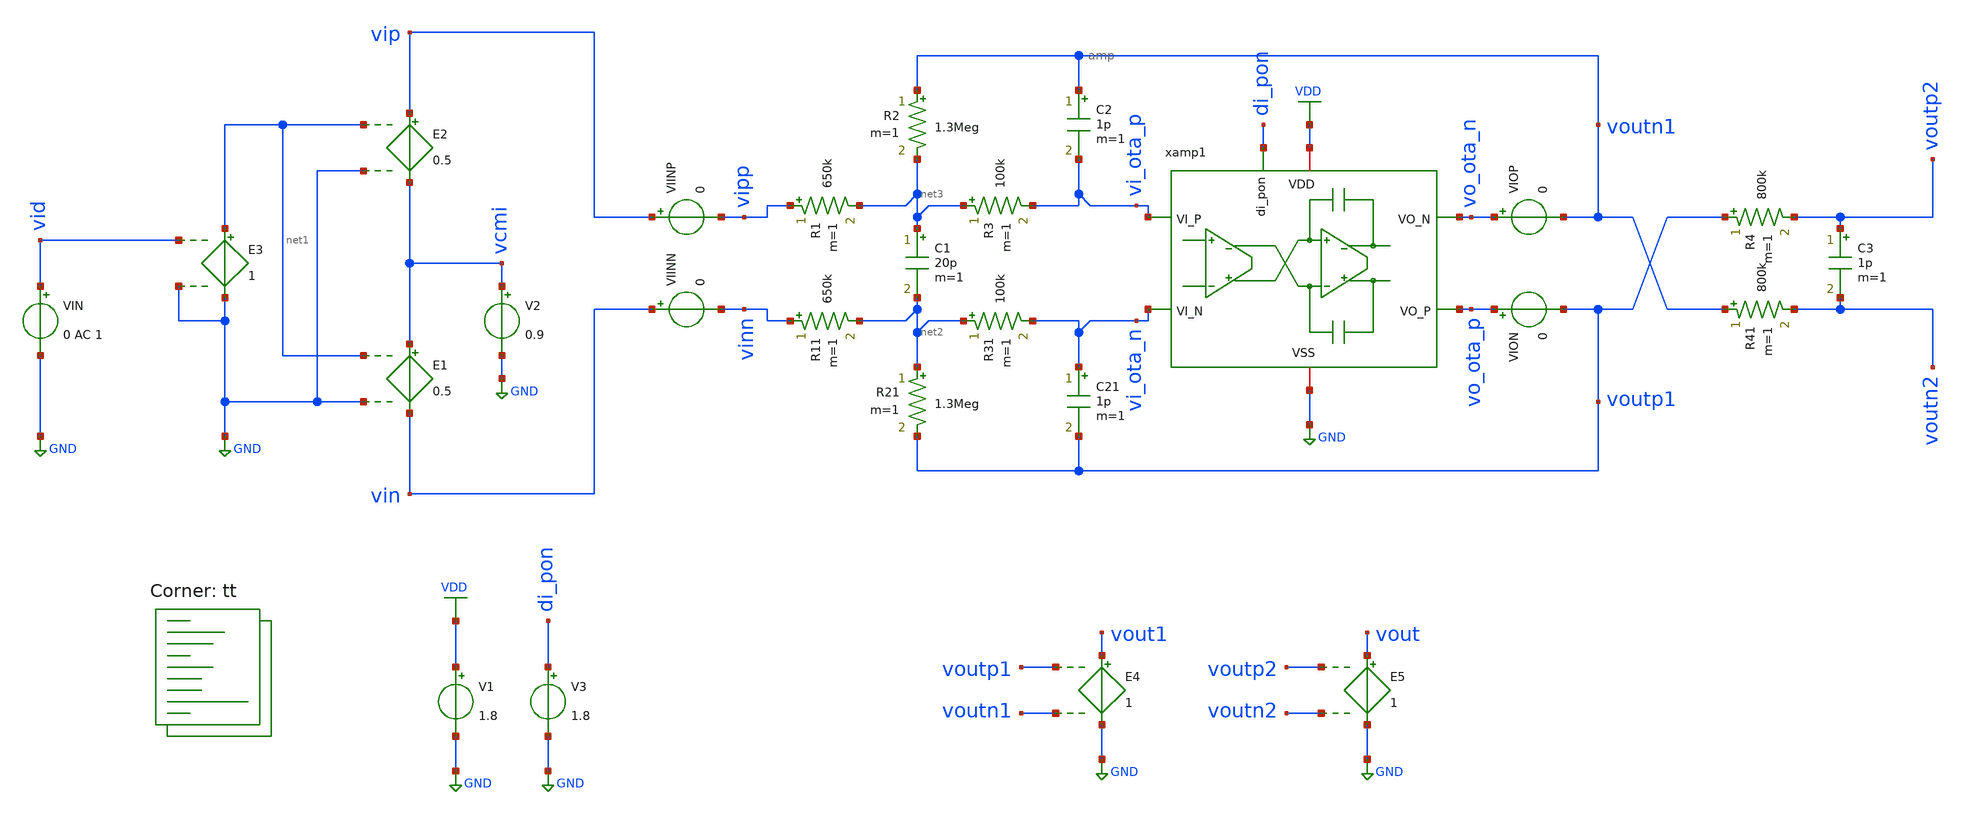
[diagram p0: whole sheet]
** sch_path: xschem/tb_filter_cl.sch
**.subckt tb_filter_cl
V2 vcmi GND 0.9
E1 vcmi vin net1 GND 0.5
E2 vip vcmi net1 GND 0.5
VIN vid GND 0 AC 1
E3 net1 GND vid GND 1
E4 vout1 GND voutp1 voutn1 1
VIINP vip vipp 0
VIINN vin vinn 0
R1 vipp net3 650k m=1
R2 voutn1 net3 1.3Meg m=1
R3 net3 vi_ota_p 100k m=1
C1 net3 net2 20p m=1
C3 voutp2 voutn2 1p m=1
R11 vinn net2 650k m=1
R21 net2 voutp1 1.3Meg m=1
R31 net2 vi_ota_n 100k m=1
C21 vi_ota_n voutp1 1p m=1
R4 voutp1 voutp2 800k m=1
R41 voutn1 voutn2 800k m=1
C2 voutn1 vi_ota_p 1p m=1
E5 vout GND voutp2 voutn2 1
VIOP vo_ota_n voutn1 0
VION vo_ota_p voutp1 0
xamp1 VDD vi_ota_n vi_ota_p vo_ota_p di_pon vo_ota_n GND amp
V1 VDD GND 1.8
V3 di_pon GND 1.8
**** begin user architecture code
.lib $::SKYWATER_MODELS/sky130.lib.spice tt


*.include /foss/designs/filter/amp_dev_save.spice
.options savecurrents
.options method=gear reltol=.005
.options sparse
.control
save all

let f_min = 10
let f_max = 100Meg
let f_stop = 500k

let Adc = 2
let err_gain_spec = 0.004
let v_step_o = 0.9
let v_step_i = v_step_o/Adc

let t_rf = 0.1u
let t_step = 50u
let t_delay = 0
let t_per = 2*t_step

let tstep = 0.1*t_rf
let tstop = 2*t_per
let tstart = t_delay

*alter @VIN[SIN] = [ 0 0.01 $&f_sig 0 0 0 ]
alter @VIN[DC] = 0.0


*set fndc = /foss/designs/frontend/frontend_dc.txt
*set fntran = /foss/designs/frontend/frontend_tran.txt
*set fnspec = /foss/designs/frontend/frontend_spec.txt
*set fnhd = /foss/designs/frontend/frontend_hd.txt
*set fnnoise = /foss/designs/frontend/frontend_noise.txt
set wr_singlescale
set wr_vecnames
option numdgt=3

set opSimOnly = 0


** Main Simulations
if $opSimOnly eq 0
	op
	ac dec 100 $&const.f_min $&const.f_max
	*set sqrnoise
	noise v(vout) VIN dec 100 $&const.f_min $&const.f_max 1
	noise v(vout) VIN dec 100 1 50Meg
	alter @VIN[PULSE] = [ 0 $&v_step_i $&t_delay $&t_rf $&t_rf $&t_step $&t_per 0 ]
	** Check power on by ramping Vdd, tie di_pon to VDD net!
	*alter @V1[PULSE] = [ 0 1.8 0 10u $&t_rf 0 0 0 ]
	tran $&tstep $&tstop $&tstart

	setplot ac1
	let A1 = v(vout1)/v(vid)
	let A2 = v(vout)/v(vid)

	let Amag_dB = vdb(A2)
	settype decibel Amag_dB
	let Aarg = 180/PI*cphase(A2)

	let fdc = const.f_min+1
	meas ac Adc_ol_dB find Amag_dB when frequency = fdc
	let Amag_fc = Adc_ol_dB-3
	meas ac fc find frequency when Amag_dB = Amag_fc
	meas ac Amin min_at Amag_dB from=const.f_min to=fc
	meas ac Amax max Amag_dB
	meas ac Astop find Amag_dB when frequency = const.f_stop

	meas ac fug find frequency when Amag_dB=0
	let err_gain_act = 1-10^(Adc_ol_dB/20)/Adc
	let Adc_ol_min = Adc*(1-err_gain_spec)/err_gain_spec
	let Adc_ol_min_dB = vdb(Adc_ol_min)
	print err_gain_act*100
	print Adc_ol_min_dB
	plot Amag_dB Aarg ylabel 'Magnitude, Phase'

	setplot noise1
	let acgain = onoise_spectrum/inoise_spectrum
	let r1 = sqrt(2)*onoise_r1
	let r2 = sqrt(2)*onoise_r2
	let r3 = sqrt(2)*onoise_r3
	let r4 = sqrt(2)*onoise_r4
	*plot inoise_spectrum ylog xlog
	plot onoise_spectrum r1 r2 r3 r4 ylog xlog ylabel 'Output Noise'

	setplot noise4
	let p_noise_q = (1e-3)^2
	let p_noise_o = onoise_total^2
	let p_sig_o = (v_step_o/(2*sqrt(2)))^2
	let snr = p_sig_o/(p_noise_o+p_noise_q)
	let snr_dB = 10*log10(snr)
	print snr_dB

	setplot tran4
	let vid = v(vid)
	let iop = viop#branch
	let ion = vion#branch
	let vcmo = (voutp1+voutn1)/2

	*plot iop ion

	plot vid vout1 vout vcmo
	plot v(vip) v(vin) v(voutp1) v(voutn1) vcmo
end

alter @VIN[DC] = 0
op

remzerovec
write tb_filter_cl.raw
.endc

**** end user architecture code
**.ends

* expanding   symbol:  /foss/designs/xschem/amp.sym # of pins=7
** sym_path: xschem/amp.sym
** sch_path: xschem/amp.sch
.subckt amp VDD VI_N VI_P VO_P di_pon VO_N VSS
*.iopin VSS
*.iopin VDD
*.ipin VI_P
*.ipin di_pon
*.ipin VI_N
*.opin VO_P
*.opin VO_N
XMP1 vbp vbp VDD VDD sky130_fd_pr__pfet_01v8 L=0.25 W='5 * 2 ' nf=2 ad='int((nf+1)/2) * W / nf * 0.29'
+ as='int((nf+2)/2) * W / nf * 0.29' pd='2*int((nf+1)/2) * (W / nf + 0.29)' ps='2*int((nf+2)/2) * (W / nf + 0.29)'
+ nrd='0.29 / W ' nrs='0.29 / W ' sa=0 sb=0 sd=0 mult=1 m=1
XMPSW3 vbp pon VDD VDD sky130_fd_pr__pfet_01v8 L=0.15 W='5 * 5 ' nf=5 ad='int((nf+1)/2) * W / nf * 0.29'
+ as='int((nf+2)/2) * W / nf * 0.29' pd='2*int((nf+1)/2) * (W / nf + 0.29)' ps='2*int((nf+2)/2) * (W / nf + 0.29)'
+ nrd='0.29 / W ' nrs='0.29 / W ' sa=0 sb=0 sd=0 mult=1 m=1
XMNSW1 pon_b di_pon VSS VSS sky130_fd_pr__nfet_01v8 L=0.15 W='3 * 1 ' nf=1 ad='int((nf+1)/2) * W / nf * 0.29'
+ as='int((nf+2)/2) * W / nf * 0.29' pd='2*int((nf+1)/2) * (W / nf + 0.29)' ps='2*int((nf+2)/2) * (W / nf + 0.29)'
+ nrd='0.29 / W ' nrs='0.29 / W ' sa=0 sb=0 sd=0 mult=1 m=1
XMPSW1 pon_b di_pon VDD VDD sky130_fd_pr__pfet_01v8 L=0.15 W='5 * 1 ' nf=1 ad='int((nf+1)/2) * W / nf * 0.29'
+ as='int((nf+2)/2) * W / nf * 0.29' pd='2*int((nf+1)/2) * (W / nf + 0.29)' ps='2*int((nf+2)/2) * (W / nf + 0.29)'
+ nrd='0.29 / W ' nrs='0.29 / W ' sa=0 sb=0 sd=0 mult=1 m=1
XMNSW2 pon pon_b VSS VSS sky130_fd_pr__nfet_01v8 L=0.15 W='3 * 3 ' nf=3 ad='int((nf+1)/2) * W / nf * 0.29'
+ as='int((nf+2)/2) * W / nf * 0.29' pd='2*int((nf+1)/2) * (W / nf + 0.29)' ps='2*int((nf+2)/2) * (W / nf + 0.29)'
+ nrd='0.29 / W ' nrs='0.29 / W ' sa=0 sb=0 sd=0 mult=1 m=1
XMPSW2 pon pon_b VDD VDD sky130_fd_pr__pfet_01v8 L=0.15 W='5 * 3 ' nf=3 ad='int((nf+1)/2) * W / nf * 0.29'
+ as='int((nf+2)/2) * W / nf * 0.29' pd='2*int((nf+1)/2) * (W / nf + 0.29)' ps='2*int((nf+2)/2) * (W / nf + 0.29)'
+ nrd='0.29 / W ' nrs='0.29 / W ' sa=0 sb=0 sd=0 mult=1 m=1
XMP2 viref1 vbp VDD VDD sky130_fd_pr__pfet_01v8 L=0.25 W='5 * 20 ' nf=20 ad='int((nf+1)/2) * W / nf * 0.29'
+ as='int((nf+2)/2) * W / nf * 0.29' pd='2*int((nf+1)/2) * (W / nf + 0.29)' ps='2*int((nf+2)/2) * (W / nf + 0.29)'
+ nrd='0.29 / W ' nrs='0.29 / W ' sa=0 sb=0 sd=0 mult=1 m=1
XC5 VDD vbp sky130_fd_pr__cap_mim_m3_1 W=5 L=5 MF=5 m=5
XMP4 vo1_n VI_P viref1 viref1 sky130_fd_pr__pfet_01v8 L=0.15 W='5 * 70 ' nf=70 ad='int((nf+1)/2) * W / nf * 0.29'
+ as='int((nf+2)/2) * W / nf * 0.29' pd='2*int((nf+1)/2) * (W / nf + 0.29)' ps='2*int((nf+2)/2) * (W / nf + 0.29)'
+ nrd='0.29 / W ' nrs='0.29 / W ' sa=0 sb=0 sd=0 mult=1 m=1
XMP5 vo1_p VI_N viref1 viref1 sky130_fd_pr__pfet_01v8 L=0.15 W='5 * 70 ' nf=70 ad='int((nf+1)/2) * W / nf * 0.29'
+ as='int((nf+2)/2) * W / nf * 0.29' pd='2*int((nf+1)/2) * (W / nf + 0.29)' ps='2*int((nf+2)/2) * (W / nf + 0.29)'
+ nrd='0.29 / W ' nrs='0.29 / W ' sa=0 sb=0 sd=0 mult=1 m=1
XMN1 vo1_n vfb1 VSS VSS sky130_fd_pr__nfet_01v8 L=1 W='3 * 6 ' nf=6 ad='int((nf+1)/2) * W / nf * 0.29'
+ as='int((nf+2)/2) * W / nf * 0.29' pd='2*int((nf+1)/2) * (W / nf + 0.29)' ps='2*int((nf+2)/2) * (W / nf + 0.29)'
+ nrd='0.29 / W ' nrs='0.29 / W ' sa=0 sb=0 sd=0 mult=1 m=1
XMN2 vo1_p vfb1 VSS VSS sky130_fd_pr__nfet_01v8 L=1 W='3 * 6 ' nf=6 ad='int((nf+1)/2) * W / nf * 0.29'
+ as='int((nf+2)/2) * W / nf * 0.29' pd='2*int((nf+1)/2) * (W / nf + 0.29)' ps='2*int((nf+2)/2) * (W / nf + 0.29)'
+ nrd='0.29 / W ' nrs='0.29 / W ' sa=0 sb=0 sd=0 mult=1 m=1
XC1 vo1_n vfb1 sky130_fd_pr__cap_mim_m3_1 W=5 L=5 MF=5 m=5
XC2 vfb1 vo1_p sky130_fd_pr__cap_mim_m3_1 W=5 L=5 MF=5 m=5
XMN3 VO_N vo1_p VSS VSS sky130_fd_pr__nfet_01v8 L=0.5 W='3 * 20 ' nf=20 ad='int((nf+1)/2) * W / nf * 0.29'
+ as='int((nf+2)/2) * W / nf * 0.29' pd='2*int((nf+1)/2) * (W / nf + 0.29)' ps='2*int((nf+2)/2) * (W / nf + 0.29)'
+ nrd='0.29 / W ' nrs='0.29 / W ' sa=0 sb=0 sd=0 mult=1 m=1
XMN4 VO_P vo1_n VSS VSS sky130_fd_pr__nfet_01v8 L=0.5 W='3 * 20 ' nf=20 ad='int((nf+1)/2) * W / nf * 0.29'
+ as='int((nf+2)/2) * W / nf * 0.29' pd='2*int((nf+1)/2) * (W / nf + 0.29)' ps='2*int((nf+2)/2) * (W / nf + 0.29)'
+ nrd='0.29 / W ' nrs='0.29 / W ' sa=0 sb=0 sd=0 mult=1 m=1
XMP3 vbncm vbp VDD VDD sky130_fd_pr__pfet_01v8 L=0.25 W='5 * 2 ' nf=2 ad='int((nf+1)/2) * W / nf * 0.29'
+ as='int((nf+2)/2) * W / nf * 0.29' pd='2*int((nf+1)/2) * (W / nf + 0.29)' ps='2*int((nf+2)/2) * (W / nf + 0.29)'
+ nrd='0.29 / W ' nrs='0.29 / W ' sa=0 sb=0 sd=0 mult=1 m=1
XMP6 VO_P vfb2 VDD VDD sky130_fd_pr__pfet_01v8 L=0.5 W='5 * 5 ' nf=5 ad='int((nf+1)/2) * W / nf * 0.29'
+ as='int((nf+2)/2) * W / nf * 0.29' pd='2*int((nf+1)/2) * (W / nf + 0.29)' ps='2*int((nf+2)/2) * (W / nf + 0.29)'
+ nrd='0.29 / W ' nrs='0.29 / W ' sa=0 sb=0 sd=0 mult=1 m=1
XMP7 VO_N vfb2 VDD VDD sky130_fd_pr__pfet_01v8 L=0.5 W='5 * 5 ' nf=5 ad='int((nf+1)/2) * W / nf * 0.29'
+ as='int((nf+2)/2) * W / nf * 0.29' pd='2*int((nf+1)/2) * (W / nf + 0.29)' ps='2*int((nf+2)/2) * (W / nf + 0.29)'
+ nrd='0.29 / W ' nrs='0.29 / W ' sa=0 sb=0 sd=0 mult=1 m=1
XC3 VO_N vfb2 sky130_fd_pr__cap_mim_m3_1 W=5 L=5 MF=5 m=5
XC4 vfb2 VO_P sky130_fd_pr__cap_mim_m3_1 W=5 L=5 MF=5 m=5
XMN5 vbncm vbncm VSS VSS sky130_fd_pr__nfet_01v8 L=0.5 W='3 * 5 ' nf=5 ad='int((nf+1)/2) * W / nf * 0.29'
+ as='int((nf+2)/2) * W / nf * 0.29' pd='2*int((nf+1)/2) * (W / nf + 0.29)' ps='2*int((nf+2)/2) * (W / nf + 0.29)'
+ nrd='0.29 / W ' nrs='0.29 / W ' sa=0 sb=0 sd=0 mult=1 m=1
XMN6 vfb2 vbncm VSS VSS sky130_fd_pr__nfet_01v8 L=0.5 W='3 * 4 ' nf=4 ad='int((nf+1)/2) * W / nf * 0.29'
+ as='int((nf+2)/2) * W / nf * 0.29' pd='2*int((nf+1)/2) * (W / nf + 0.29)' ps='2*int((nf+2)/2) * (W / nf + 0.29)'
+ nrd='0.29 / W ' nrs='0.29 / W ' sa=0 sb=0 sd=0 mult=1 m=1
XMNSW3 vrref_sw pon VSS VSS sky130_fd_pr__nfet_01v8 L=0.15 W='3 * 5 ' nf=5 ad='int((nf+1)/2) * W / nf * 0.29'
+ as='int((nf+2)/2) * W / nf * 0.29' pd='2*int((nf+1)/2) * (W / nf + 0.29)' ps='2*int((nf+2)/2) * (W / nf + 0.29)'
+ nrd='0.29 / W ' nrs='0.29 / W ' sa=0 sb=0 sd=0 mult=1 m=1
XRREF vrref_sw vbp VSS sky130_fd_pr__res_xhigh_po_0p35 L=5.6 mult=1 m=1
xr1 vfb1 vo1_n vo1_p VSS rstring_cm
xr2 vfb2 VO_P VO_N VSS rstring_cm
XC6 vo1_p VO_N sky130_fd_pr__cap_mim_m3_1 W=5 L=5 MF=16 m=16
XC7 vo1_n VO_P sky130_fd_pr__cap_mim_m3_1 W=5 L=5 MF=16 m=16
.ends


* expanding   symbol:  /foss/designs/xschem/rstring_cm.sym # of pins=4
** sym_path: xschem/rstring_cm.sym
** sch_path: xschem/rstring_cm.sch
.subckt rstring_cm VR_M VR_N VR_P VSS
*.iopin VSS
*.ipin VR_P
*.ipin VR_N
*.opin VR_M
XR1 VR_P net1 VSS sky130_fd_pr__res_xhigh_po_0p35 L=5.6 mult=1 m=1
XR2 net1 VR_M VSS sky130_fd_pr__res_xhigh_po_0p35 L=5.6 mult=1 m=1
XR3 VR_M net2 VSS sky130_fd_pr__res_xhigh_po_0p35 L=5.6 mult=1 m=1
XR4 net2 VR_N VSS sky130_fd_pr__res_xhigh_po_0p35 L=5.6 mult=1 m=1
.ends

.GLOBAL GND
.GLOBAL VDD
.end
